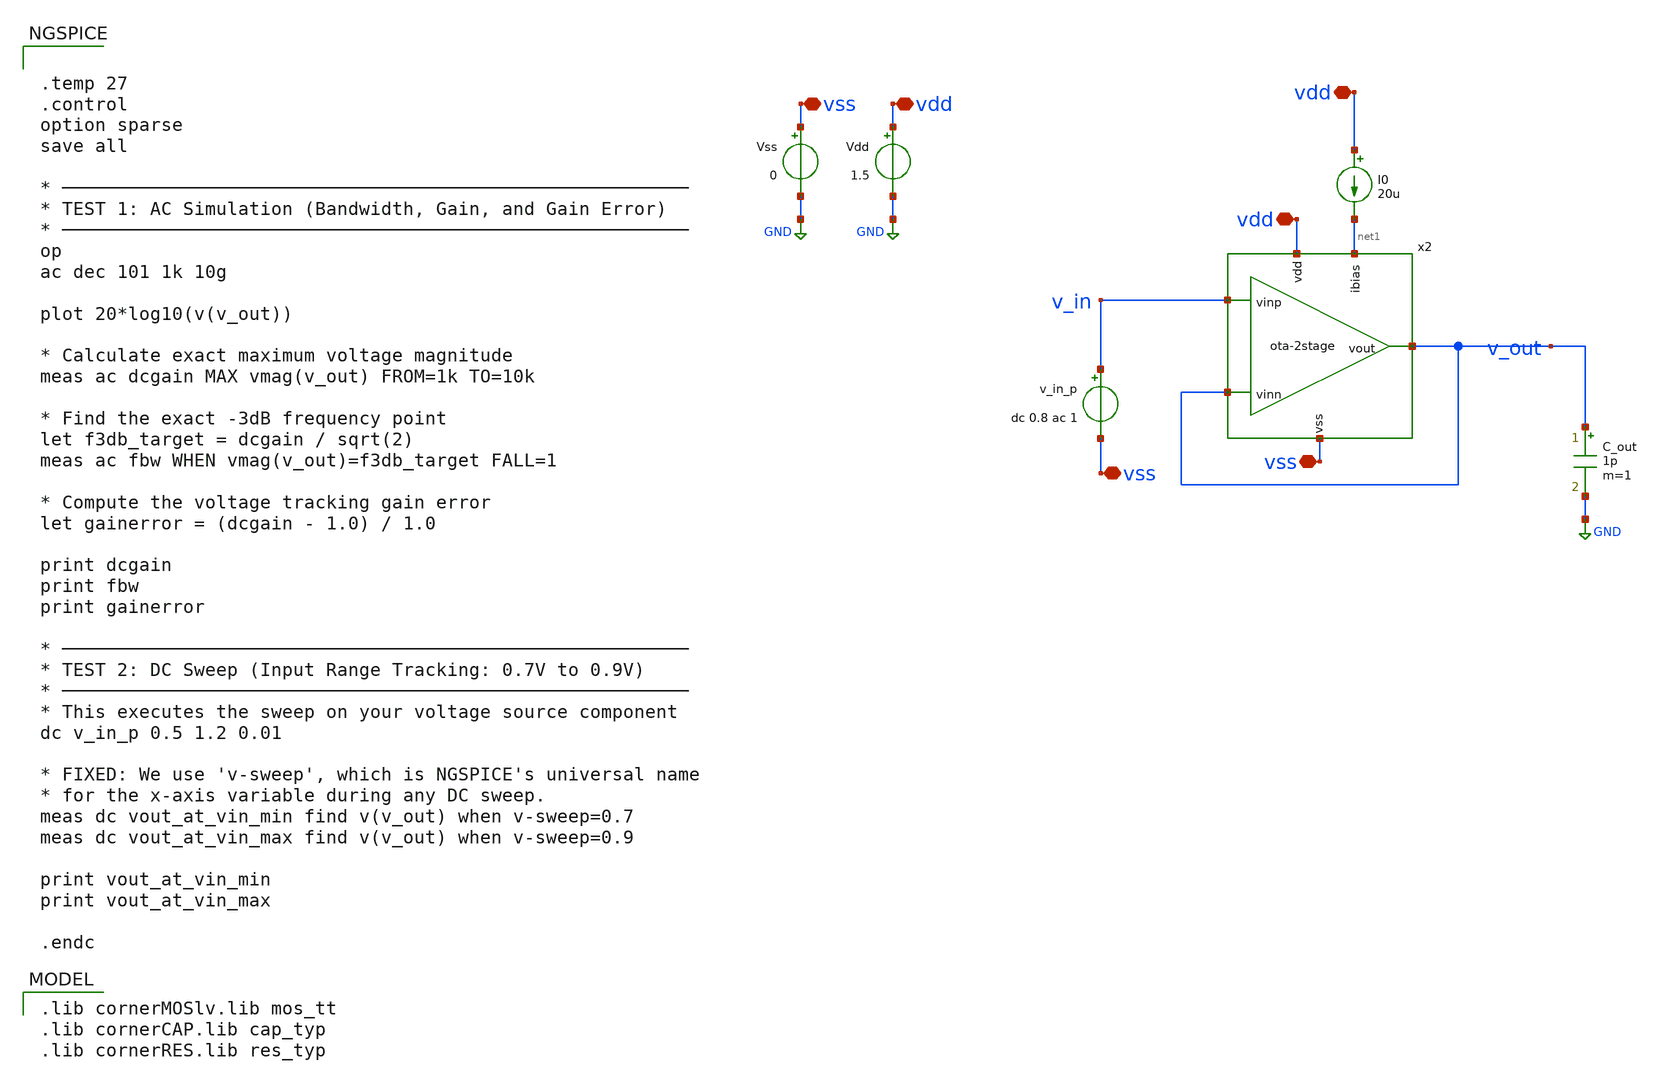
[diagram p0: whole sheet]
** sch_path: teshbench/ota-2stage_tb-vb.sch
**.subckt ota-2stage_tb-vb vss vdd vss vdd vdd vss
*.iopin vss
*.iopin vdd
*.iopin vss
*.iopin vdd
*.iopin vdd
*.iopin vss
I0 vdd net1 20u
Vdd vdd GND 1.5
Vss vss GND 0
v_in_p v_in vss dc 0.8 ac 1
C_out v_out GND 1p m=1
x2 vdd net1 v_out v_out v_in vss ota-2stage
**** begin user architecture code


.temp 27
.control
option sparse
save all

* ─────────────────────────────────────────────────────────
* TEST 1: AC Simulation (Bandwidth, Gain, and Gain Error)
* ─────────────────────────────────────────────────────────
op
ac dec 101 1k 10g

plot 20*log10(v(v_out))

* Calculate exact maximum voltage magnitude
meas ac dcgain MAX vmag(v_out) FROM=1k TO=10k

* Find the exact -3dB frequency point
let f3db_target = dcgain / sqrt(2)
meas ac fbw WHEN vmag(v_out)=f3db_target FALL=1

* Compute the voltage tracking gain error
let gainerror = (dcgain - 1.0) / 1.0

print dcgain
print fbw
print gainerror

* ─────────────────────────────────────────────────────────
* TEST 2: DC Sweep (Input Range Tracking: 0.7V to 0.9V)
* ─────────────────────────────────────────────────────────
* This executes the sweep on your voltage source component
dc v_in_p 0.5 1.2 0.01

* FIXED: We use 'v-sweep', which is NGSPICE's universal name
* for the x-axis variable during any DC sweep.
meas dc vout_at_vin_min find v(v_out) when v-sweep=0.7
meas dc vout_at_vin_max find v(v_out) when v-sweep=0.9

print vout_at_vin_min
print vout_at_vin_max

.endc


 .lib cornerMOSlv.lib mos_tt
.lib cornerCAP.lib cap_typ
.lib cornerRES.lib res_typ

**** end user architecture code
**.ends
.GLOBAL GND
.end
